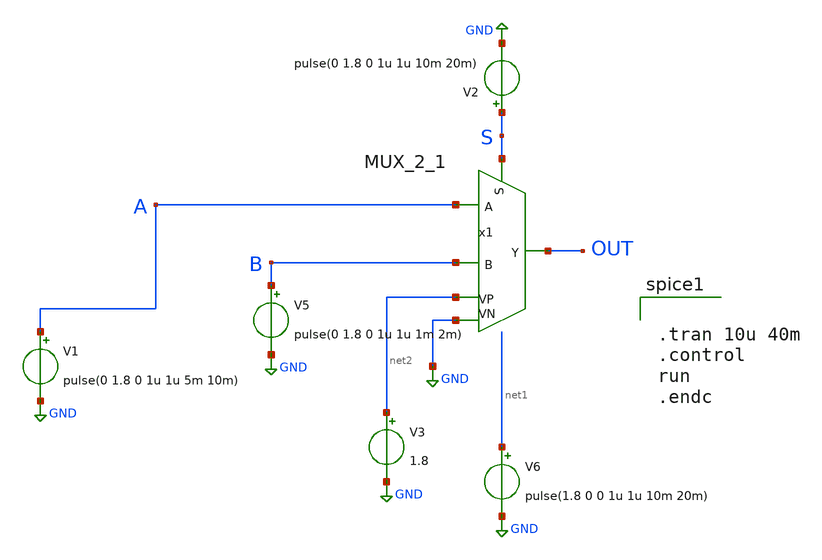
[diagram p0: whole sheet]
** sch_path: ADC/16bit_C2C/MagicAndSpice/EE431_FinalProj/mux_tb.sch
**.subckt mux_tb
V5 B GND pulse(0 1.8 0 1u 1u 1m 2m)
V6 net1 GND pulse(1.8 0 0 1u 1u 10m 20m)
x1 A B S OUT net2 GND MUX_2_1
V1 A GND pulse(0 1.8 0 1u 1u 5m 10m)
V2 S GND pulse(0 1.8 0 1u 1u 10m 20m)
V3 net2 GND 1.8
**** begin user architecture code
 .lib $::SKYWATER_MODELS/sky130.lib.spice tt


.tran 10u 40m
.control
run
.endc

**** end user architecture code
**.ends
.GLOBAL GND
.end
